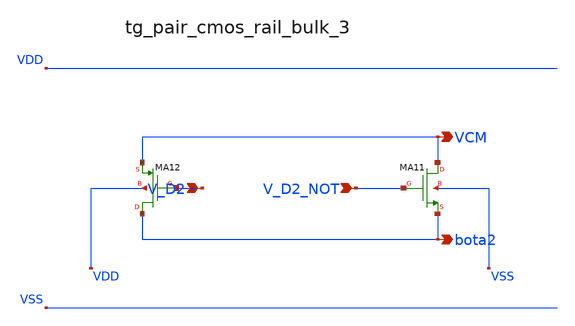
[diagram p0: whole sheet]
** sch_path: analog-db/raw/ia_005_hsu_pga_ideal/hier/blocks/tg_pair_cmos_rail_bulk_3.sch
**.subckt tg_pair_cmos_rail_bulk_3 V_D2 V_D2_NOT VCM bota2
*.ipin V_D2
*.ipin V_D2_NOT
*.opin VCM
*.opin bota2
XMA11 VCM V_D2_NOT bota2 VSS sg13_lv_nmos w=x_dut_xma11_w l=x_dut_xma11_l ng=1 m=x_dut_xma11_m
XMA12 bota2 V_D2 VCM VDD sg13_lv_pmos w=x_dut_xma12_w l=x_dut_xma12_l ng=1 m=x_dut_xma12_m
**.ends
.end
